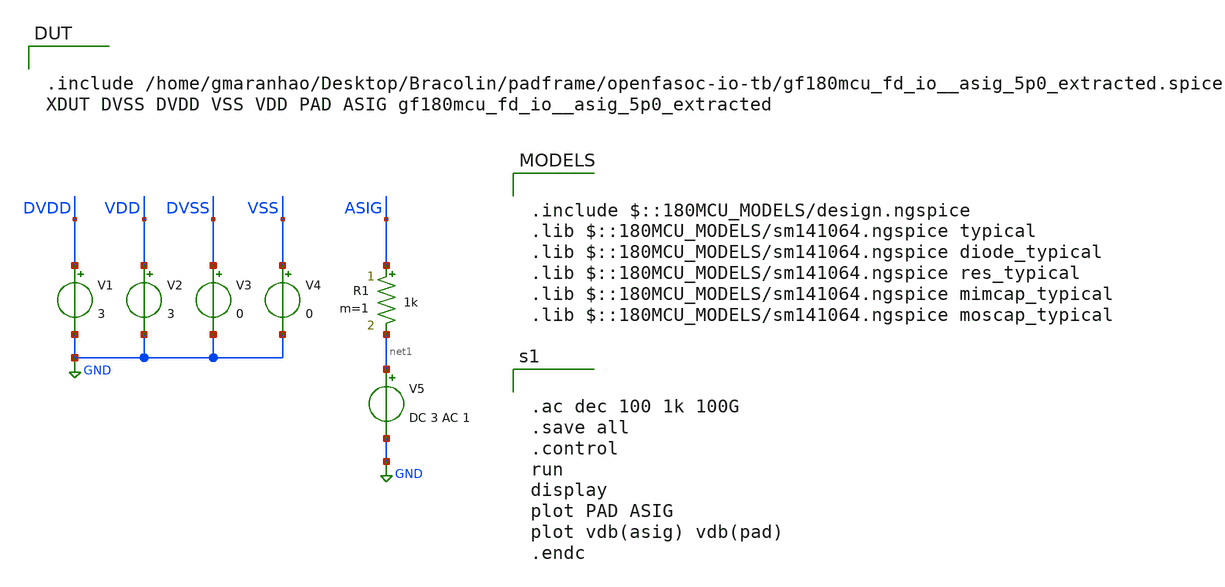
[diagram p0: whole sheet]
** sch_path: padframe/openfasoc-io-tb/analog_io_ac_pex.sch
**.subckt analog_io_ac_pex
V1 DVDD GND 3
V2 VDD GND 3
V3 DVSS GND 0
V4 VSS GND 0
V5 net1 GND DC 3 AC 1
R1 ASIG net1 1k m=1
**** begin user architecture code


.ac dec 100 1k 100G
.save all
.control
run
display
plot PAD ASIG
plot vdb(asig) vdb(pad)
.endc



.include $::180MCU_MODELS/design.ngspice
.lib $::180MCU_MODELS/sm141064.ngspice typical
.lib $::180MCU_MODELS/sm141064.ngspice diode_typical
.lib $::180MCU_MODELS/sm141064.ngspice res_typical
.lib $::180MCU_MODELS/sm141064.ngspice mimcap_typical
.lib $::180MCU_MODELS/sm141064.ngspice moscap_typical


.include /home/gmaranhao/Desktop/Bracolin/padframe/openfasoc-io-tb/gf180mcu_fd_io__asig_5p0_extracted.spice
XDUT DVSS DVDD VSS VDD PAD ASIG gf180mcu_fd_io__asig_5p0_extracted

**** end user architecture code
**.ends
.GLOBAL GND
.end
